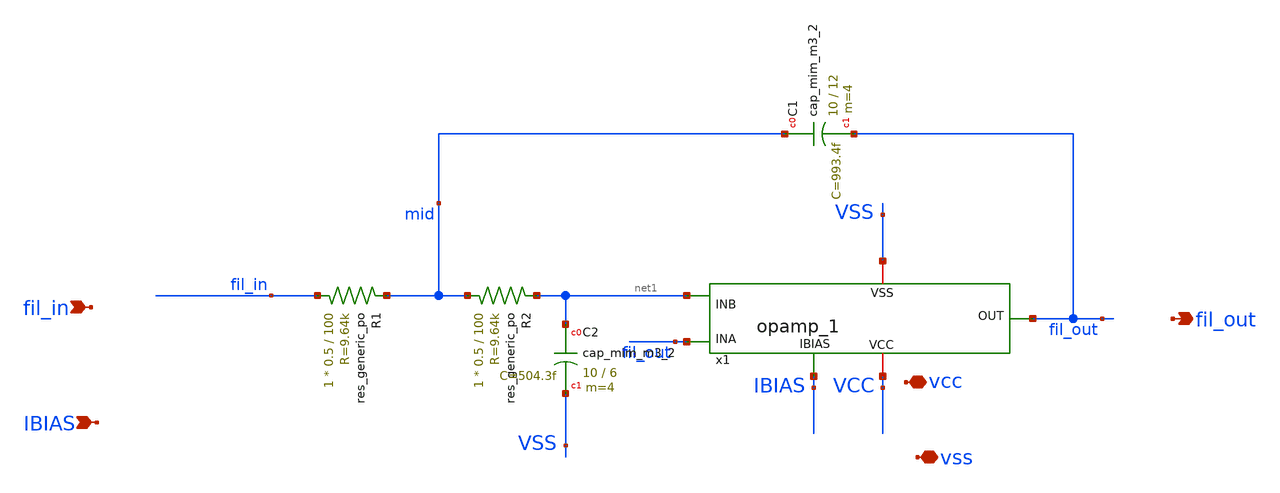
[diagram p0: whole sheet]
** sch_path: xschem/filter22M.sch
**.subckt filter22M fil_out fil_in vcc vss IBIAS
*.opin fil_out
*.ipin fil_in
*.iopin vcc
*.iopin vss
*.ipin IBIAS
x1 VCC fil_out fil_out net1 VSS IBIAS opamp_1
XR1 fil_in mid sky130_fd_pr__res_generic_po W=0.5 L=100 m=1
XR2 mid net1 sky130_fd_pr__res_generic_po W=0.5 L=100 m=1
XC1 mid fil_out sky130_fd_pr__cap_mim_m3_2 W=10 L=12 MF=4 m=4
XC2 net1 VSS sky130_fd_pr__cap_mim_m3_2 W=10 L=6 MF=4 m=4
**.ends

* expanding   symbol:  opamp_1.sym # of pins=6
** sym_path: xschem/opamp_1.sym
** sch_path: xschem/opamp_1.sch
.subckt opamp_1 VCC OUT INA INB VSS IBIAS
*.ipin INA
*.ipin INB
*.opin OUT
*.iopin VCC
*.iopin VSS
*.ipin IBIAS
XM1 MIRR INA TAILV VSS sky130_fd_pr__nfet_01v8 L=1 W=20 nf=1 ad='int((nf+1)/2) * W/nf * 0.29' as='int((nf+2)/2) * W/nf * 0.29'
+ pd='2*int((nf+1)/2) * (W/nf + 0.29)' ps='2*int((nf+2)/2) * (W/nf + 0.29)' nrd='0.29 / W' nrs='0.29 / W'
+ sa=0 sb=0 sd=0 mult=1 m=1
XM2 DIFF_OUT INB TAILV VSS sky130_fd_pr__nfet_01v8 L=1 W=20 nf=1 ad='int((nf+1)/2) * W/nf * 0.29' as='int((nf+2)/2) * W/nf * 0.29'
+ pd='2*int((nf+1)/2) * (W/nf + 0.29)' ps='2*int((nf+2)/2) * (W/nf + 0.29)' nrd='0.29 / W' nrs='0.29 / W'
+ sa=0 sb=0 sd=0 mult=1 m=1
XM3 TAILV IBIAS VSS VSS sky130_fd_pr__nfet_01v8 L=1 W=40 nf=1 ad='int((nf+1)/2) * W/nf * 0.29' as='int((nf+2)/2) * W/nf * 0.29'
+ pd='2*int((nf+1)/2) * (W/nf + 0.29)' ps='2*int((nf+2)/2) * (W/nf + 0.29)' nrd='0.29 / W' nrs='0.29 / W'
+ sa=0 sb=0 sd=0 mult=1 m=1
XM4 MIRR MIRR VCC VCC sky130_fd_pr__pfet_01v8_lvt L=0.5 W=14 nf=1 ad='int((nf+1)/2) * W/nf * 0.29' as='int((nf+2)/2) * W/nf * 0.29'
+ pd='2*int((nf+1)/2) * (W/nf + 0.29)' ps='2*int((nf+2)/2) * (W/nf + 0.29)' nrd='0.29 / W' nrs='0.29 / W'
+ sa=0 sb=0 sd=0 mult=1 m=1
XM5 DIFF_OUT MIRR VCC VCC sky130_fd_pr__pfet_01v8_lvt L=0.5 W=14 nf=1 ad='int((nf+1)/2) * W/nf * 0.29'
+ as='int((nf+2)/2) * W/nf * 0.29' pd='2*int((nf+1)/2) * (W/nf + 0.29)' ps='2*int((nf+2)/2) * (W/nf + 0.29)'
+ nrd='0.29 / W' nrs='0.29 / W' sa=0 sb=0 sd=0 mult=1 m=1
XM6 OUT IBIAS VSS VSS sky130_fd_pr__nfet_01v8 L=0.5 W=93 nf=1 ad='int((nf+1)/2) * W/nf * 0.29' as='int((nf+2)/2) * W/nf * 0.29'
+ pd='2*int((nf+1)/2) * (W/nf + 0.29)' ps='2*int((nf+2)/2) * (W/nf + 0.29)' nrd='0.29 / W' nrs='0.29 / W'
+ sa=0 sb=0 sd=0 mult=1 m=1
XM7 OUT DIFF_OUT VCC VCC sky130_fd_pr__pfet_01v8_lvt L=0.5 W=70 nf=1 ad='int((nf+1)/2) * W/nf * 0.29'
+ as='int((nf+2)/2) * W/nf * 0.29' pd='2*int((nf+1)/2) * (W/nf + 0.29)' ps='2*int((nf+2)/2) * (W/nf + 0.29)'
+ nrd='0.29 / W' nrs='0.29 / W' sa=0 sb=0 sd=0 mult=1 m=1
XM9 RBIAS IBIAS VSS VSS sky130_fd_pr__nfet_01v8 L=1 W=5 nf=1 ad='int((nf+1)/2) * W/nf * 0.29' as='int((nf+2)/2) * W/nf * 0.29'
+ pd='2*int((nf+1)/2) * (W/nf + 0.29)' ps='2*int((nf+2)/2) * (W/nf + 0.29)' nrd='0.29 / W' nrs='0.29 / W'
+ sa=0 sb=0 sd=0 mult=1 m=1
XM10 RBIAS RBIAS net2 VCC sky130_fd_pr__pfet_01v8_lvt L=0.5 W=1 nf=1 ad='int((nf+1)/2) * W/nf * 0.29'
+ as='int((nf+2)/2) * W/nf * 0.29' pd='2*int((nf+1)/2) * (W/nf + 0.29)' ps='2*int((nf+2)/2) * (W/nf + 0.29)'
+ nrd='0.29 / W' nrs='0.29 / W' sa=0 sb=0 sd=0 mult=1 m=1
XM11 net2 net2 VCC VCC sky130_fd_pr__pfet_01v8_lvt L=0.5 W=7.5 nf=1 ad='int((nf+1)/2) * W/nf * 0.29'
+ as='int((nf+2)/2) * W/nf * 0.29' pd='2*int((nf+1)/2) * (W/nf + 0.29)' ps='2*int((nf+2)/2) * (W/nf + 0.29)'
+ nrd='0.29 / W' nrs='0.29 / W' sa=0 sb=0 sd=0 mult=1 m=1
XC1 OUT net1 sky130_fd_pr__cap_mim_m3_2 W=20 L=13 MF=1 m=1
XM8 net1 RBIAS DIFF_OUT VCC sky130_fd_pr__pfet_01v8_lvt L=0.5 W=14 nf=1 ad='int((nf+1)/2) * W/nf * 0.29'
+ as='int((nf+2)/2) * W/nf * 0.29' pd='2*int((nf+1)/2) * (W/nf + 0.29)' ps='2*int((nf+2)/2) * (W/nf + 0.29)'
+ nrd='0.29 / W' nrs='0.29 / W' sa=0 sb=0 sd=0 mult=1 m=1
.ends

.end
